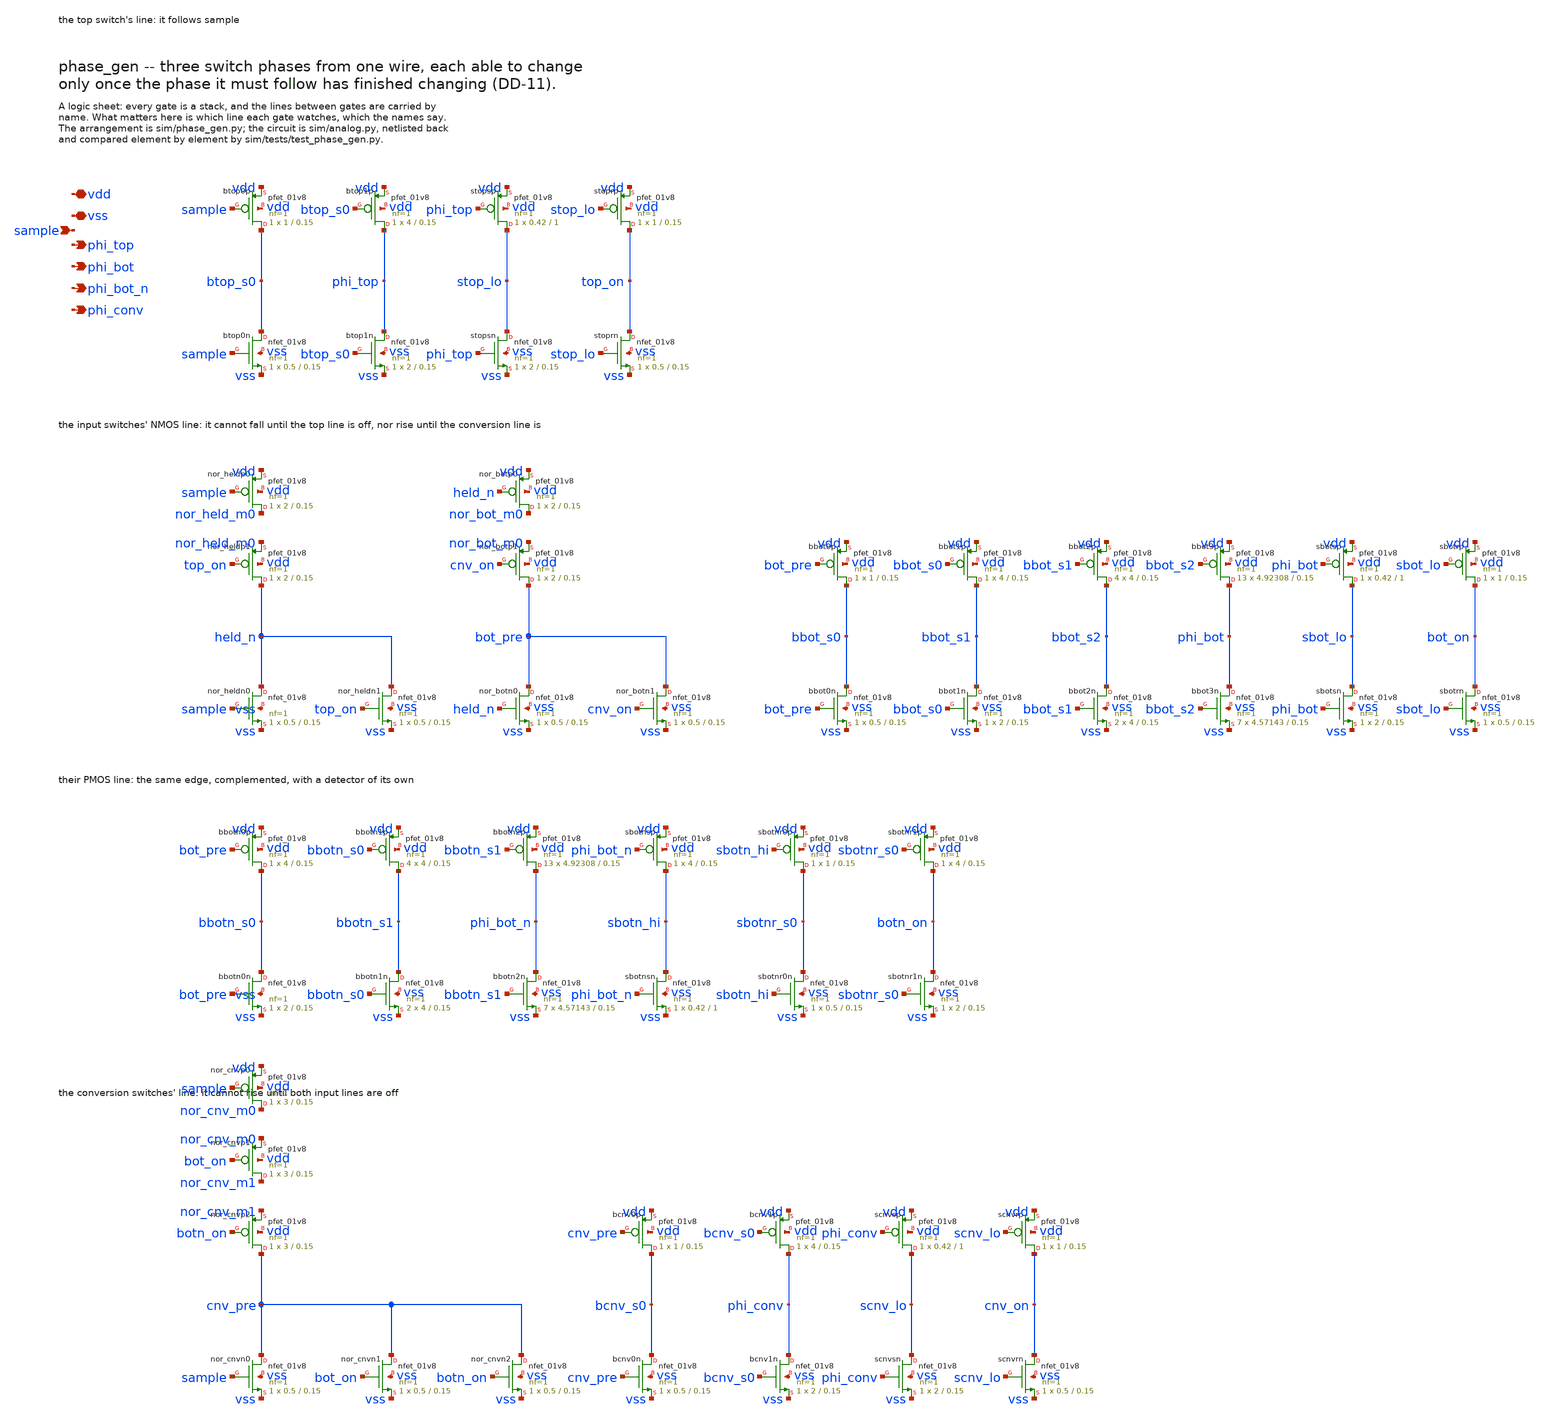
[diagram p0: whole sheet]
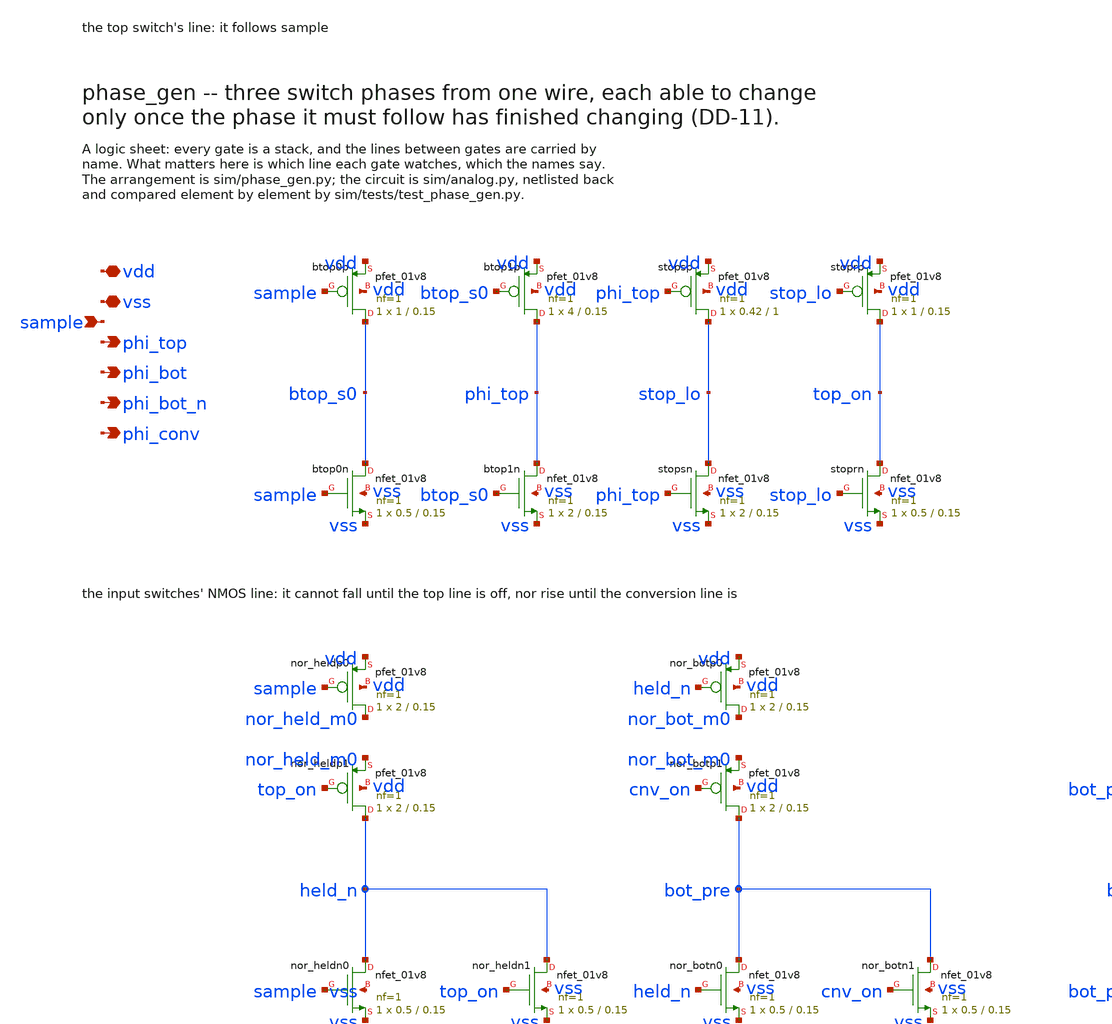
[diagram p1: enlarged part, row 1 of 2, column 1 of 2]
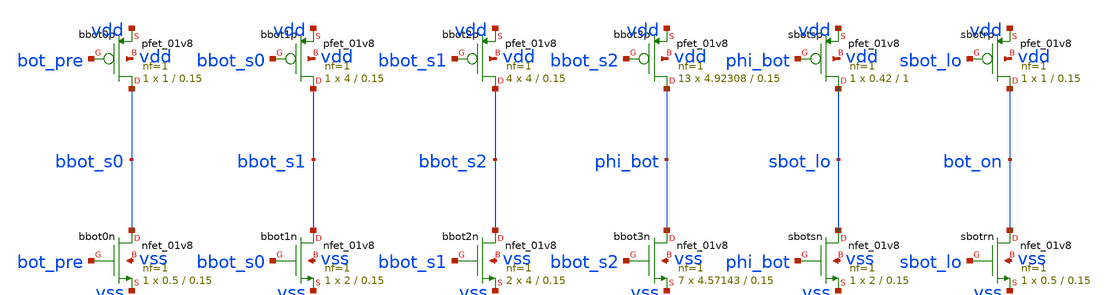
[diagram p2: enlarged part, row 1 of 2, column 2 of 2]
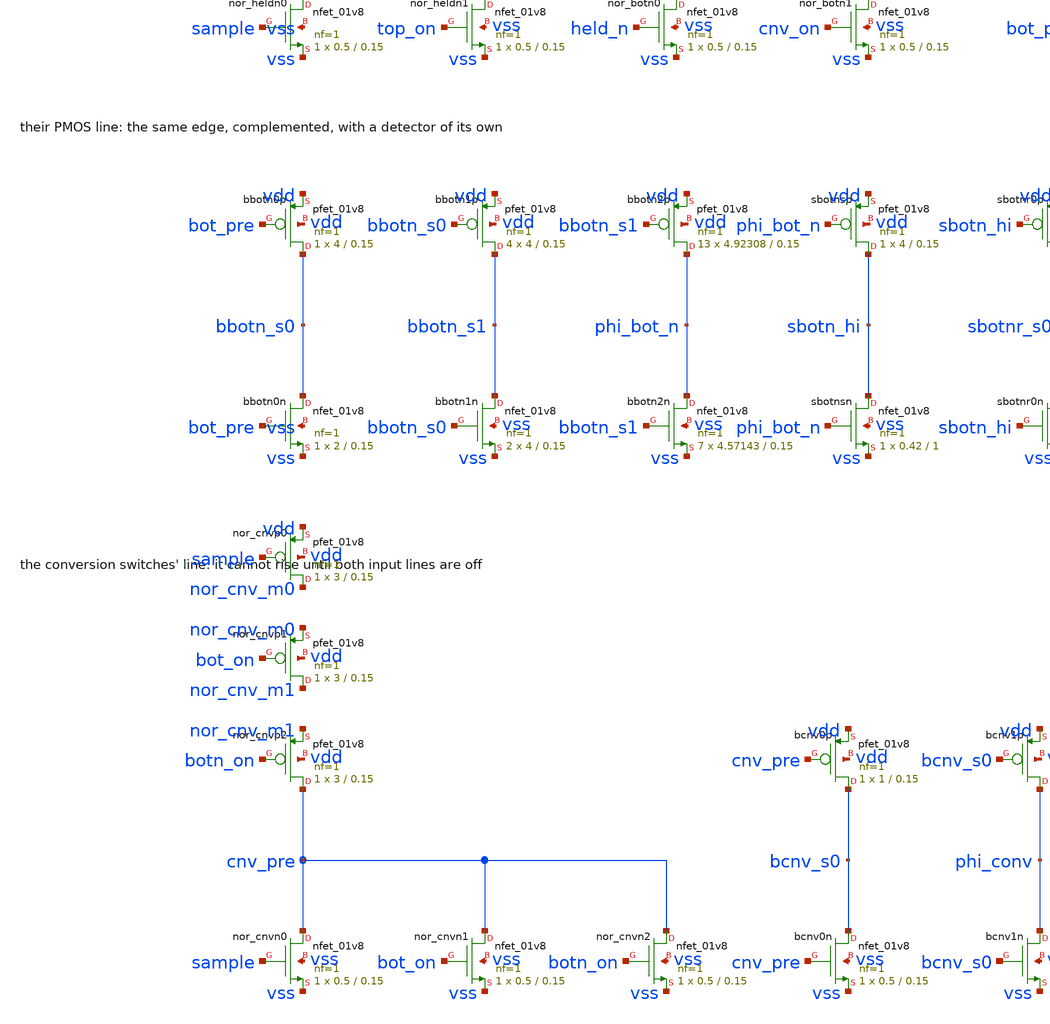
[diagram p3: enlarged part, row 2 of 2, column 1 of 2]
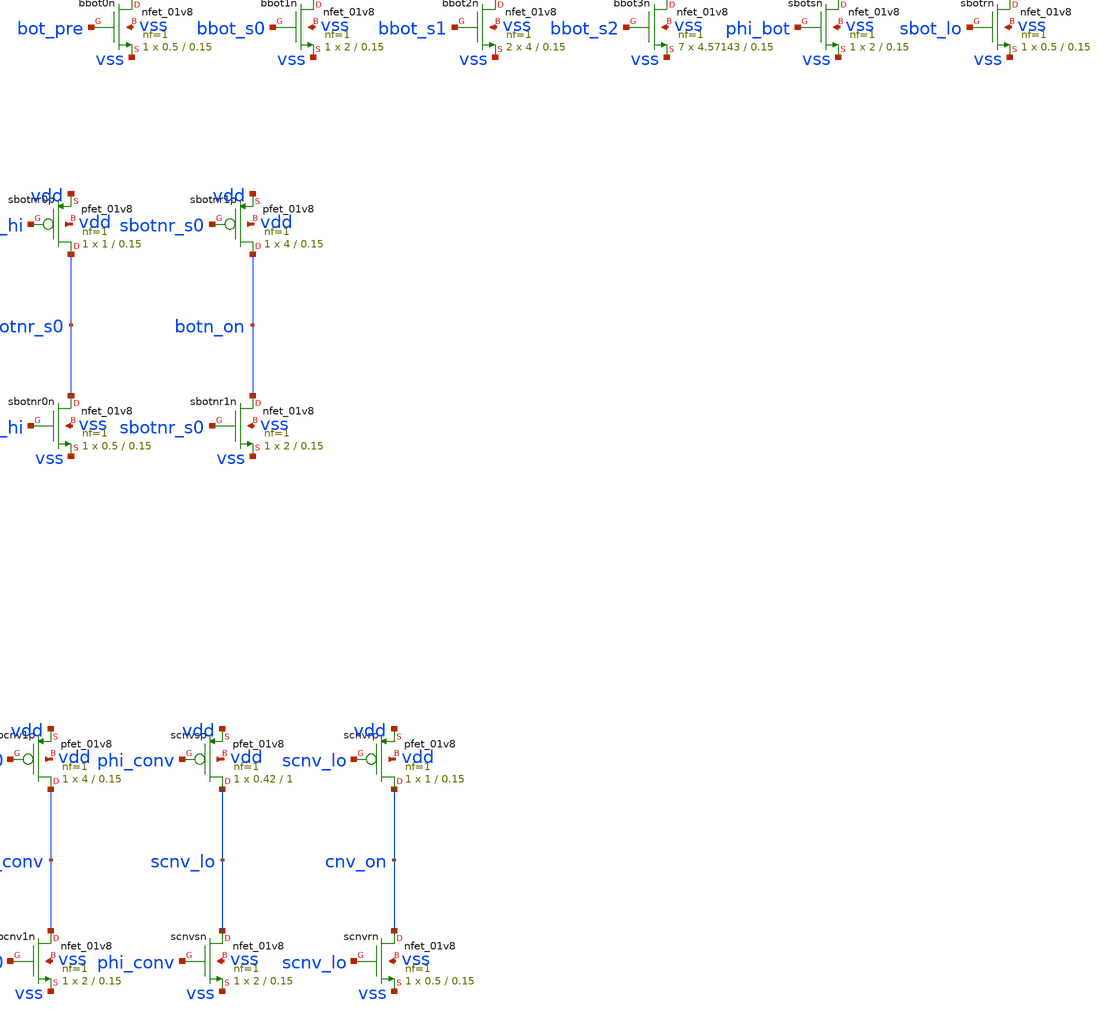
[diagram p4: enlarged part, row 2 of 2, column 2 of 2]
** sch_path: xschem/phase_gen.sch
**.subckt phase_gen vdd vss sample phi_top phi_bot phi_bot_n phi_conv
*.iopin vdd
*.iopin vss
*.ipin sample
*.opin phi_top
*.opin phi_bot
*.opin phi_bot_n
*.opin phi_conv
Xbtop0p btop_s0 sample vdd vdd sky130_fd_pr__pfet_01v8 L=0.15 W=1 nf=1 ad='int((nf+1)/2) * W/nf * 0.29'
+ as='int((nf+2)/2) * W/nf * 0.29' pd='2*int((nf+1)/2) * (W/nf + 0.29)' ps='2*int((nf+2)/2) * (W/nf + 0.29)'
+ nrd='0.29 / W' nrs='0.29 / W' sa=0 sb=0 sd=0 mult=1 m=1
Xbtop0n btop_s0 sample vss vss sky130_fd_pr__nfet_01v8 L=0.15 W=0.5 nf=1 ad='int((1 + 1)/2) * 0.5 / 1 * 0.29'
+ as='int((1 + 2)/2) * 0.5 / 1 * 0.29' pd='2*int((1 + 1)/2) * (0.5 / 1 + 0.29)' ps='2*int((1 + 2)/2) * (0.5 / 1 + 0.29)'
+ nrd='0.29 / 0.5 ' nrs='0.29 / 0.5 ' sa=0 sb=0 sd=0 mult=1 m=1
Xbtop1p phi_top btop_s0 vdd vdd sky130_fd_pr__pfet_01v8 L=0.15 W=4 nf=1 ad='int((nf+1)/2) * W/nf * 0.29'
+ as='int((nf+2)/2) * W/nf * 0.29' pd='2*int((nf+1)/2) * (W/nf + 0.29)' ps='2*int((nf+2)/2) * (W/nf + 0.29)'
+ nrd='0.29 / W' nrs='0.29 / W' sa=0 sb=0 sd=0 mult=1 m=1
Xbtop1n phi_top btop_s0 vss vss sky130_fd_pr__nfet_01v8 L=0.15 W=2 nf=1 ad='int((1 + 1)/2) * 2 / 1 * 0.29'
+ as='int((1 + 2)/2) * 2 / 1 * 0.29' pd='2*int((1 + 1)/2) * (2 / 1 + 0.29)' ps='2*int((1 + 2)/2) * (2 / 1 + 0.29)'
+ nrd='0.29 / 2 ' nrs='0.29 / 2 ' sa=0 sb=0 sd=0 mult=1 m=1
Xstopsp stop_lo phi_top vdd vdd sky130_fd_pr__pfet_01v8 L=1 W=0.42 nf=1 ad='int((nf+1)/2) * W/nf * 0.29'
+ as='int((nf+2)/2) * W/nf * 0.29' pd='2*int((nf+1)/2) * (W/nf + 0.29)' ps='2*int((nf+2)/2) * (W/nf + 0.29)'
+ nrd='0.29 / W' nrs='0.29 / W' sa=0 sb=0 sd=0 mult=1 m=1
Xstopsn stop_lo phi_top vss vss sky130_fd_pr__nfet_01v8 L=0.15 W=2 nf=1 ad='int((1 + 1)/2) * 2 / 1 * 0.29'
+ as='int((1 + 2)/2) * 2 / 1 * 0.29' pd='2*int((1 + 1)/2) * (2 / 1 + 0.29)' ps='2*int((1 + 2)/2) * (2 / 1 + 0.29)'
+ nrd='0.29 / 2 ' nrs='0.29 / 2 ' sa=0 sb=0 sd=0 mult=1 m=1
Xstoprp top_on stop_lo vdd vdd sky130_fd_pr__pfet_01v8 L=0.15 W=1 nf=1 ad='int((nf+1)/2) * W/nf * 0.29'
+ as='int((nf+2)/2) * W/nf * 0.29' pd='2*int((nf+1)/2) * (W/nf + 0.29)' ps='2*int((nf+2)/2) * (W/nf + 0.29)'
+ nrd='0.29 / W' nrs='0.29 / W' sa=0 sb=0 sd=0 mult=1 m=1
Xstoprn top_on stop_lo vss vss sky130_fd_pr__nfet_01v8 L=0.15 W=0.5 nf=1 ad='int((1 + 1)/2) * 0.5 / 1 * 0.29'
+ as='int((1 + 2)/2) * 0.5 / 1 * 0.29' pd='2*int((1 + 1)/2) * (0.5 / 1 + 0.29)' ps='2*int((1 + 2)/2) * (0.5 / 1 + 0.29)'
+ nrd='0.29 / 0.5 ' nrs='0.29 / 0.5 ' sa=0 sb=0 sd=0 mult=1 m=1
Xnor_heldp0 nor_held_m0 sample vdd vdd sky130_fd_pr__pfet_01v8 L=0.15 W=2 nf=1 ad='int((nf+1)/2) * W/nf * 0.29'
+ as='int((nf+2)/2) * W/nf * 0.29' pd='2*int((nf+1)/2) * (W/nf + 0.29)' ps='2*int((nf+2)/2) * (W/nf + 0.29)'
+ nrd='0.29 / W' nrs='0.29 / W' sa=0 sb=0 sd=0 mult=1 m=1
Xnor_heldp1 held_n top_on nor_held_m0 vdd sky130_fd_pr__pfet_01v8 L=0.15 W=2 nf=1 ad='int((nf+1)/2) * W/nf * 0.29'
+ as='int((nf+2)/2) * W/nf * 0.29' pd='2*int((nf+1)/2) * (W/nf + 0.29)' ps='2*int((nf+2)/2) * (W/nf + 0.29)'
+ nrd='0.29 / W' nrs='0.29 / W' sa=0 sb=0 sd=0 mult=1 m=1
Xnor_heldn0 held_n sample vss vss sky130_fd_pr__nfet_01v8 L=0.15 W=0.5 nf=1 ad='int((1 + 1)/2) * 0.5 / 1 * 0.29'
+ as='int((1 + 2)/2) * 0.5 / 1 * 0.29' pd='2*int((1 + 1)/2) * (0.5 / 1 + 0.29)' ps='2*int((1 + 2)/2) * (0.5 / 1 + 0.29)'
+ nrd='0.29 / 0.5 ' nrs='0.29 / 0.5 ' sa=0 sb=0 sd=0 mult=1 m=1
Xnor_heldn1 held_n top_on vss vss sky130_fd_pr__nfet_01v8 L=0.15 W=0.5 nf=1 ad='int((1 + 1)/2) * 0.5 / 1 * 0.29'
+ as='int((1 + 2)/2) * 0.5 / 1 * 0.29' pd='2*int((1 + 1)/2) * (0.5 / 1 + 0.29)' ps='2*int((1 + 2)/2) * (0.5 / 1 + 0.29)'
+ nrd='0.29 / 0.5 ' nrs='0.29 / 0.5 ' sa=0 sb=0 sd=0 mult=1 m=1
Xnor_botp0 nor_bot_m0 held_n vdd vdd sky130_fd_pr__pfet_01v8 L=0.15 W=2 nf=1 ad='int((nf+1)/2) * W/nf * 0.29'
+ as='int((nf+2)/2) * W/nf * 0.29' pd='2*int((nf+1)/2) * (W/nf + 0.29)' ps='2*int((nf+2)/2) * (W/nf + 0.29)'
+ nrd='0.29 / W' nrs='0.29 / W' sa=0 sb=0 sd=0 mult=1 m=1
Xnor_botp1 bot_pre cnv_on nor_bot_m0 vdd sky130_fd_pr__pfet_01v8 L=0.15 W=2 nf=1 ad='int((nf+1)/2) * W/nf * 0.29'
+ as='int((nf+2)/2) * W/nf * 0.29' pd='2*int((nf+1)/2) * (W/nf + 0.29)' ps='2*int((nf+2)/2) * (W/nf + 0.29)'
+ nrd='0.29 / W' nrs='0.29 / W' sa=0 sb=0 sd=0 mult=1 m=1
Xnor_botn0 bot_pre held_n vss vss sky130_fd_pr__nfet_01v8 L=0.15 W=0.5 nf=1 ad='int((1 + 1)/2) * 0.5 / 1 * 0.29'
+ as='int((1 + 2)/2) * 0.5 / 1 * 0.29' pd='2*int((1 + 1)/2) * (0.5 / 1 + 0.29)' ps='2*int((1 + 2)/2) * (0.5 / 1 + 0.29)'
+ nrd='0.29 / 0.5 ' nrs='0.29 / 0.5 ' sa=0 sb=0 sd=0 mult=1 m=1
Xnor_botn1 bot_pre cnv_on vss vss sky130_fd_pr__nfet_01v8 L=0.15 W=0.5 nf=1 ad='int((1 + 1)/2) * 0.5 / 1 * 0.29'
+ as='int((1 + 2)/2) * 0.5 / 1 * 0.29' pd='2*int((1 + 1)/2) * (0.5 / 1 + 0.29)' ps='2*int((1 + 2)/2) * (0.5 / 1 + 0.29)'
+ nrd='0.29 / 0.5 ' nrs='0.29 / 0.5 ' sa=0 sb=0 sd=0 mult=1 m=1
Xbbot0p bbot_s0 bot_pre vdd vdd sky130_fd_pr__pfet_01v8 L=0.15 W=1 nf=1 ad='int((nf+1)/2) * W/nf * 0.29'
+ as='int((nf+2)/2) * W/nf * 0.29' pd='2*int((nf+1)/2) * (W/nf + 0.29)' ps='2*int((nf+2)/2) * (W/nf + 0.29)'
+ nrd='0.29 / W' nrs='0.29 / W' sa=0 sb=0 sd=0 mult=1 m=1
Xbbot0n bbot_s0 bot_pre vss vss sky130_fd_pr__nfet_01v8 L=0.15 W=0.5 nf=1 ad='int((1 + 1)/2) * 0.5 / 1 * 0.29'
+ as='int((1 + 2)/2) * 0.5 / 1 * 0.29' pd='2*int((1 + 1)/2) * (0.5 / 1 + 0.29)' ps='2*int((1 + 2)/2) * (0.5 / 1 + 0.29)'
+ nrd='0.29 / 0.5 ' nrs='0.29 / 0.5 ' sa=0 sb=0 sd=0 mult=1 m=1
Xbbot1p bbot_s1 bbot_s0 vdd vdd sky130_fd_pr__pfet_01v8 L=0.15 W=4 nf=1 ad='int((nf+1)/2) * W/nf * 0.29'
+ as='int((nf+2)/2) * W/nf * 0.29' pd='2*int((nf+1)/2) * (W/nf + 0.29)' ps='2*int((nf+2)/2) * (W/nf + 0.29)'
+ nrd='0.29 / W' nrs='0.29 / W' sa=0 sb=0 sd=0 mult=1 m=1
Xbbot1n bbot_s1 bbot_s0 vss vss sky130_fd_pr__nfet_01v8 L=0.15 W=2 nf=1 ad='int((1 + 1)/2) * 2 / 1 * 0.29'
+ as='int((1 + 2)/2) * 2 / 1 * 0.29' pd='2*int((1 + 1)/2) * (2 / 1 + 0.29)' ps='2*int((1 + 2)/2) * (2 / 1 + 0.29)'
+ nrd='0.29 / 2 ' nrs='0.29 / 2 ' sa=0 sb=0 sd=0 mult=1 m=1
Xbbot2p bbot_s2 bbot_s1 vdd vdd sky130_fd_pr__pfet_01v8 L=0.15 W=4 nf=1 ad='int((nf+1)/2) * W/nf * 0.29'
+ as='int((nf+2)/2) * W/nf * 0.29' pd='2*int((nf+1)/2) * (W/nf + 0.29)' ps='2*int((nf+2)/2) * (W/nf + 0.29)'
+ nrd='0.29 / W' nrs='0.29 / W' sa=0 sb=0 sd=0 mult=4 m=4
Xbbot2n bbot_s2 bbot_s1 vss vss sky130_fd_pr__nfet_01v8 L=0.15 W=4 nf=1 ad='int((1 + 1)/2) * 4 / 1 * 0.29'
+ as='int((1 + 2)/2) * 4 / 1 * 0.29' pd='2*int((1 + 1)/2) * (4 / 1 + 0.29)' ps='2*int((1 + 2)/2) * (4 / 1 + 0.29)'
+ nrd='0.29 / 4 ' nrs='0.29 / 4 ' sa=0 sb=0 sd=0 mult=2 m=2
Xbbot3p phi_bot bbot_s2 vdd vdd sky130_fd_pr__pfet_01v8 L=0.15 W=4.92308 nf=1 ad='int((nf+1)/2) * W/nf * 0.29'
+ as='int((nf+2)/2) * W/nf * 0.29' pd='2*int((nf+1)/2) * (W/nf + 0.29)' ps='2*int((nf+2)/2) * (W/nf + 0.29)'
+ nrd='0.29 / W' nrs='0.29 / W' sa=0 sb=0 sd=0 mult=13 m=13
Xbbot3n phi_bot bbot_s2 vss vss sky130_fd_pr__nfet_01v8 L=0.15 W=4.57143 nf=1 ad='int((1 + 1)/2) * 4.57143 / 1 * 0.29'
+ as='int((1 + 2)/2) * 4.57143 / 1 * 0.29' pd='2*int((1 + 1)/2) * (4.57143 / 1 + 0.29)' ps='2*int((1 + 2)/2) * (4.57143 / 1 + 0.29)'
+ nrd='0.29 / 4.57143 ' nrs='0.29 / 4.57143 ' sa=0 sb=0 sd=0 mult=7 m=7
Xsbotsp sbot_lo phi_bot vdd vdd sky130_fd_pr__pfet_01v8 L=1 W=0.42 nf=1 ad='int((nf+1)/2) * W/nf * 0.29'
+ as='int((nf+2)/2) * W/nf * 0.29' pd='2*int((nf+1)/2) * (W/nf + 0.29)' ps='2*int((nf+2)/2) * (W/nf + 0.29)'
+ nrd='0.29 / W' nrs='0.29 / W' sa=0 sb=0 sd=0 mult=1 m=1
Xsbotsn sbot_lo phi_bot vss vss sky130_fd_pr__nfet_01v8 L=0.15 W=2 nf=1 ad='int((1 + 1)/2) * 2 / 1 * 0.29'
+ as='int((1 + 2)/2) * 2 / 1 * 0.29' pd='2*int((1 + 1)/2) * (2 / 1 + 0.29)' ps='2*int((1 + 2)/2) * (2 / 1 + 0.29)'
+ nrd='0.29 / 2 ' nrs='0.29 / 2 ' sa=0 sb=0 sd=0 mult=1 m=1
Xsbotrp bot_on sbot_lo vdd vdd sky130_fd_pr__pfet_01v8 L=0.15 W=1 nf=1 ad='int((nf+1)/2) * W/nf * 0.29'
+ as='int((nf+2)/2) * W/nf * 0.29' pd='2*int((nf+1)/2) * (W/nf + 0.29)' ps='2*int((nf+2)/2) * (W/nf + 0.29)'
+ nrd='0.29 / W' nrs='0.29 / W' sa=0 sb=0 sd=0 mult=1 m=1
Xsbotrn bot_on sbot_lo vss vss sky130_fd_pr__nfet_01v8 L=0.15 W=0.5 nf=1 ad='int((1 + 1)/2) * 0.5 / 1 * 0.29'
+ as='int((1 + 2)/2) * 0.5 / 1 * 0.29' pd='2*int((1 + 1)/2) * (0.5 / 1 + 0.29)' ps='2*int((1 + 2)/2) * (0.5 / 1 + 0.29)'
+ nrd='0.29 / 0.5 ' nrs='0.29 / 0.5 ' sa=0 sb=0 sd=0 mult=1 m=1
Xbbotn0p bbotn_s0 bot_pre vdd vdd sky130_fd_pr__pfet_01v8 L=0.15 W=4 nf=1 ad='int((nf+1)/2) * W/nf * 0.29'
+ as='int((nf+2)/2) * W/nf * 0.29' pd='2*int((nf+1)/2) * (W/nf + 0.29)' ps='2*int((nf+2)/2) * (W/nf + 0.29)'
+ nrd='0.29 / W' nrs='0.29 / W' sa=0 sb=0 sd=0 mult=1 m=1
Xbbotn0n bbotn_s0 bot_pre vss vss sky130_fd_pr__nfet_01v8 L=0.15 W=2 nf=1 ad='int((1 + 1)/2) * 2 / 1 * 0.29'
+ as='int((1 + 2)/2) * 2 / 1 * 0.29' pd='2*int((1 + 1)/2) * (2 / 1 + 0.29)' ps='2*int((1 + 2)/2) * (2 / 1 + 0.29)'
+ nrd='0.29 / 2 ' nrs='0.29 / 2 ' sa=0 sb=0 sd=0 mult=1 m=1
Xbbotn1p bbotn_s1 bbotn_s0 vdd vdd sky130_fd_pr__pfet_01v8 L=0.15 W=4 nf=1 ad='int((nf+1)/2) * W/nf * 0.29'
+ as='int((nf+2)/2) * W/nf * 0.29' pd='2*int((nf+1)/2) * (W/nf + 0.29)' ps='2*int((nf+2)/2) * (W/nf + 0.29)'
+ nrd='0.29 / W' nrs='0.29 / W' sa=0 sb=0 sd=0 mult=4 m=4
Xbbotn1n bbotn_s1 bbotn_s0 vss vss sky130_fd_pr__nfet_01v8 L=0.15 W=4 nf=1 ad='int((1 + 1)/2) * 4 / 1 * 0.29'
+ as='int((1 + 2)/2) * 4 / 1 * 0.29' pd='2*int((1 + 1)/2) * (4 / 1 + 0.29)' ps='2*int((1 + 2)/2) * (4 / 1 + 0.29)'
+ nrd='0.29 / 4 ' nrs='0.29 / 4 ' sa=0 sb=0 sd=0 mult=2 m=2
Xbbotn2p phi_bot_n bbotn_s1 vdd vdd sky130_fd_pr__pfet_01v8 L=0.15 W=4.92308 nf=1 ad='int((nf+1)/2) * W/nf * 0.29'
+ as='int((nf+2)/2) * W/nf * 0.29' pd='2*int((nf+1)/2) * (W/nf + 0.29)' ps='2*int((nf+2)/2) * (W/nf + 0.29)'
+ nrd='0.29 / W' nrs='0.29 / W' sa=0 sb=0 sd=0 mult=13 m=13
Xbbotn2n phi_bot_n bbotn_s1 vss vss sky130_fd_pr__nfet_01v8 L=0.15 W=4.57143 nf=1 ad='int((1 + 1)/2) * 4.57143 / 1 * 0.29'
+ as='int((1 + 2)/2) * 4.57143 / 1 * 0.29' pd='2*int((1 + 1)/2) * (4.57143 / 1 + 0.29)' ps='2*int((1 + 2)/2) * (4.57143 / 1 + 0.29)'
+ nrd='0.29 / 4.57143 ' nrs='0.29 / 4.57143 ' sa=0 sb=0 sd=0 mult=7 m=7
Xsbotnsp sbotn_hi phi_bot_n vdd vdd sky130_fd_pr__pfet_01v8 L=0.15 W=4 nf=1 ad='int((nf+1)/2) * W/nf * 0.29'
+ as='int((nf+2)/2) * W/nf * 0.29' pd='2*int((nf+1)/2) * (W/nf + 0.29)' ps='2*int((nf+2)/2) * (W/nf + 0.29)'
+ nrd='0.29 / W' nrs='0.29 / W' sa=0 sb=0 sd=0 mult=1 m=1
Xsbotnsn sbotn_hi phi_bot_n vss vss sky130_fd_pr__nfet_01v8 L=1 W=0.42 nf=1 ad='int((1 + 1)/2) * 0.42 / 1 * 0.29'
+ as='int((1 + 2)/2) * 0.42 / 1 * 0.29' pd='2*int((1 + 1)/2) * (0.42 / 1 + 0.29)' ps='2*int((1 + 2)/2) * (0.42 / 1 + 0.29)'
+ nrd='0.29 / 0.42 ' nrs='0.29 / 0.42 ' sa=0 sb=0 sd=0 mult=1 m=1
Xsbotnr0p sbotnr_s0 sbotn_hi vdd vdd sky130_fd_pr__pfet_01v8 L=0.15 W=1 nf=1 ad='int((nf+1)/2) * W/nf * 0.29'
+ as='int((nf+2)/2) * W/nf * 0.29' pd='2*int((nf+1)/2) * (W/nf + 0.29)' ps='2*int((nf+2)/2) * (W/nf + 0.29)'
+ nrd='0.29 / W' nrs='0.29 / W' sa=0 sb=0 sd=0 mult=1 m=1
Xsbotnr0n sbotnr_s0 sbotn_hi vss vss sky130_fd_pr__nfet_01v8 L=0.15 W=0.5 nf=1 ad='int((1 + 1)/2) * 0.5 / 1 * 0.29'
+ as='int((1 + 2)/2) * 0.5 / 1 * 0.29' pd='2*int((1 + 1)/2) * (0.5 / 1 + 0.29)' ps='2*int((1 + 2)/2) * (0.5 / 1 + 0.29)'
+ nrd='0.29 / 0.5 ' nrs='0.29 / 0.5 ' sa=0 sb=0 sd=0 mult=1 m=1
Xsbotnr1p botn_on sbotnr_s0 vdd vdd sky130_fd_pr__pfet_01v8 L=0.15 W=4 nf=1 ad='int((nf+1)/2) * W/nf * 0.29'
+ as='int((nf+2)/2) * W/nf * 0.29' pd='2*int((nf+1)/2) * (W/nf + 0.29)' ps='2*int((nf+2)/2) * (W/nf + 0.29)'
+ nrd='0.29 / W' nrs='0.29 / W' sa=0 sb=0 sd=0 mult=1 m=1
Xsbotnr1n botn_on sbotnr_s0 vss vss sky130_fd_pr__nfet_01v8 L=0.15 W=2 nf=1 ad='int((1 + 1)/2) * 2 / 1 * 0.29'
+ as='int((1 + 2)/2) * 2 / 1 * 0.29' pd='2*int((1 + 1)/2) * (2 / 1 + 0.29)' ps='2*int((1 + 2)/2) * (2 / 1 + 0.29)'
+ nrd='0.29 / 2 ' nrs='0.29 / 2 ' sa=0 sb=0 sd=0 mult=1 m=1
Xnor_cnvp0 nor_cnv_m0 sample vdd vdd sky130_fd_pr__pfet_01v8 L=0.15 W=3 nf=1 ad='int((nf+1)/2) * W/nf * 0.29'
+ as='int((nf+2)/2) * W/nf * 0.29' pd='2*int((nf+1)/2) * (W/nf + 0.29)' ps='2*int((nf+2)/2) * (W/nf + 0.29)'
+ nrd='0.29 / W' nrs='0.29 / W' sa=0 sb=0 sd=0 mult=1 m=1
Xnor_cnvp1 nor_cnv_m1 bot_on nor_cnv_m0 vdd sky130_fd_pr__pfet_01v8 L=0.15 W=3 nf=1 ad='int((nf+1)/2) * W/nf * 0.29'
+ as='int((nf+2)/2) * W/nf * 0.29' pd='2*int((nf+1)/2) * (W/nf + 0.29)' ps='2*int((nf+2)/2) * (W/nf + 0.29)'
+ nrd='0.29 / W' nrs='0.29 / W' sa=0 sb=0 sd=0 mult=1 m=1
Xnor_cnvp2 cnv_pre botn_on nor_cnv_m1 vdd sky130_fd_pr__pfet_01v8 L=0.15 W=3 nf=1 ad='int((nf+1)/2) * W/nf * 0.29'
+ as='int((nf+2)/2) * W/nf * 0.29' pd='2*int((nf+1)/2) * (W/nf + 0.29)' ps='2*int((nf+2)/2) * (W/nf + 0.29)'
+ nrd='0.29 / W' nrs='0.29 / W' sa=0 sb=0 sd=0 mult=1 m=1
Xnor_cnvn0 cnv_pre sample vss vss sky130_fd_pr__nfet_01v8 L=0.15 W=0.5 nf=1 ad='int((1 + 1)/2) * 0.5 / 1 * 0.29'
+ as='int((1 + 2)/2) * 0.5 / 1 * 0.29' pd='2*int((1 + 1)/2) * (0.5 / 1 + 0.29)' ps='2*int((1 + 2)/2) * (0.5 / 1 + 0.29)'
+ nrd='0.29 / 0.5 ' nrs='0.29 / 0.5 ' sa=0 sb=0 sd=0 mult=1 m=1
Xnor_cnvn1 cnv_pre bot_on vss vss sky130_fd_pr__nfet_01v8 L=0.15 W=0.5 nf=1 ad='int((1 + 1)/2) * 0.5 / 1 * 0.29'
+ as='int((1 + 2)/2) * 0.5 / 1 * 0.29' pd='2*int((1 + 1)/2) * (0.5 / 1 + 0.29)' ps='2*int((1 + 2)/2) * (0.5 / 1 + 0.29)'
+ nrd='0.29 / 0.5 ' nrs='0.29 / 0.5 ' sa=0 sb=0 sd=0 mult=1 m=1
Xnor_cnvn2 cnv_pre botn_on vss vss sky130_fd_pr__nfet_01v8 L=0.15 W=0.5 nf=1 ad='int((1 + 1)/2) * 0.5 / 1 * 0.29'
+ as='int((1 + 2)/2) * 0.5 / 1 * 0.29' pd='2*int((1 + 1)/2) * (0.5 / 1 + 0.29)' ps='2*int((1 + 2)/2) * (0.5 / 1 + 0.29)'
+ nrd='0.29 / 0.5 ' nrs='0.29 / 0.5 ' sa=0 sb=0 sd=0 mult=1 m=1
Xbcnv0p bcnv_s0 cnv_pre vdd vdd sky130_fd_pr__pfet_01v8 L=0.15 W=1 nf=1 ad='int((nf+1)/2) * W/nf * 0.29'
+ as='int((nf+2)/2) * W/nf * 0.29' pd='2*int((nf+1)/2) * (W/nf + 0.29)' ps='2*int((nf+2)/2) * (W/nf + 0.29)'
+ nrd='0.29 / W' nrs='0.29 / W' sa=0 sb=0 sd=0 mult=1 m=1
Xbcnv0n bcnv_s0 cnv_pre vss vss sky130_fd_pr__nfet_01v8 L=0.15 W=0.5 nf=1 ad='int((1 + 1)/2) * 0.5 / 1 * 0.29'
+ as='int((1 + 2)/2) * 0.5 / 1 * 0.29' pd='2*int((1 + 1)/2) * (0.5 / 1 + 0.29)' ps='2*int((1 + 2)/2) * (0.5 / 1 + 0.29)'
+ nrd='0.29 / 0.5 ' nrs='0.29 / 0.5 ' sa=0 sb=0 sd=0 mult=1 m=1
Xbcnv1p phi_conv bcnv_s0 vdd vdd sky130_fd_pr__pfet_01v8 L=0.15 W=4 nf=1 ad='int((nf+1)/2) * W/nf * 0.29'
+ as='int((nf+2)/2) * W/nf * 0.29' pd='2*int((nf+1)/2) * (W/nf + 0.29)' ps='2*int((nf+2)/2) * (W/nf + 0.29)'
+ nrd='0.29 / W' nrs='0.29 / W' sa=0 sb=0 sd=0 mult=1 m=1
Xbcnv1n phi_conv bcnv_s0 vss vss sky130_fd_pr__nfet_01v8 L=0.15 W=2 nf=1 ad='int((1 + 1)/2) * 2 / 1 * 0.29'
+ as='int((1 + 2)/2) * 2 / 1 * 0.29' pd='2*int((1 + 1)/2) * (2 / 1 + 0.29)' ps='2*int((1 + 2)/2) * (2 / 1 + 0.29)'
+ nrd='0.29 / 2 ' nrs='0.29 / 2 ' sa=0 sb=0 sd=0 mult=1 m=1
Xscnvsp scnv_lo phi_conv vdd vdd sky130_fd_pr__pfet_01v8 L=1 W=0.42 nf=1 ad='int((nf+1)/2) * W/nf * 0.29'
+ as='int((nf+2)/2) * W/nf * 0.29' pd='2*int((nf+1)/2) * (W/nf + 0.29)' ps='2*int((nf+2)/2) * (W/nf + 0.29)'
+ nrd='0.29 / W' nrs='0.29 / W' sa=0 sb=0 sd=0 mult=1 m=1
Xscnvsn scnv_lo phi_conv vss vss sky130_fd_pr__nfet_01v8 L=0.15 W=2 nf=1 ad='int((1 + 1)/2) * 2 / 1 * 0.29'
+ as='int((1 + 2)/2) * 2 / 1 * 0.29' pd='2*int((1 + 1)/2) * (2 / 1 + 0.29)' ps='2*int((1 + 2)/2) * (2 / 1 + 0.29)'
+ nrd='0.29 / 2 ' nrs='0.29 / 2 ' sa=0 sb=0 sd=0 mult=1 m=1
Xscnvrp cnv_on scnv_lo vdd vdd sky130_fd_pr__pfet_01v8 L=0.15 W=1 nf=1 ad='int((nf+1)/2) * W/nf * 0.29'
+ as='int((nf+2)/2) * W/nf * 0.29' pd='2*int((nf+1)/2) * (W/nf + 0.29)' ps='2*int((nf+2)/2) * (W/nf + 0.29)'
+ nrd='0.29 / W' nrs='0.29 / W' sa=0 sb=0 sd=0 mult=1 m=1
Xscnvrn cnv_on scnv_lo vss vss sky130_fd_pr__nfet_01v8 L=0.15 W=0.5 nf=1 ad='int((1 + 1)/2) * 0.5 / 1 * 0.29'
+ as='int((1 + 2)/2) * 0.5 / 1 * 0.29' pd='2*int((1 + 1)/2) * (0.5 / 1 + 0.29)' ps='2*int((1 + 2)/2) * (0.5 / 1 + 0.29)'
+ nrd='0.29 / 0.5 ' nrs='0.29 / 0.5 ' sa=0 sb=0 sd=0 mult=1 m=1
**.ends
.end
